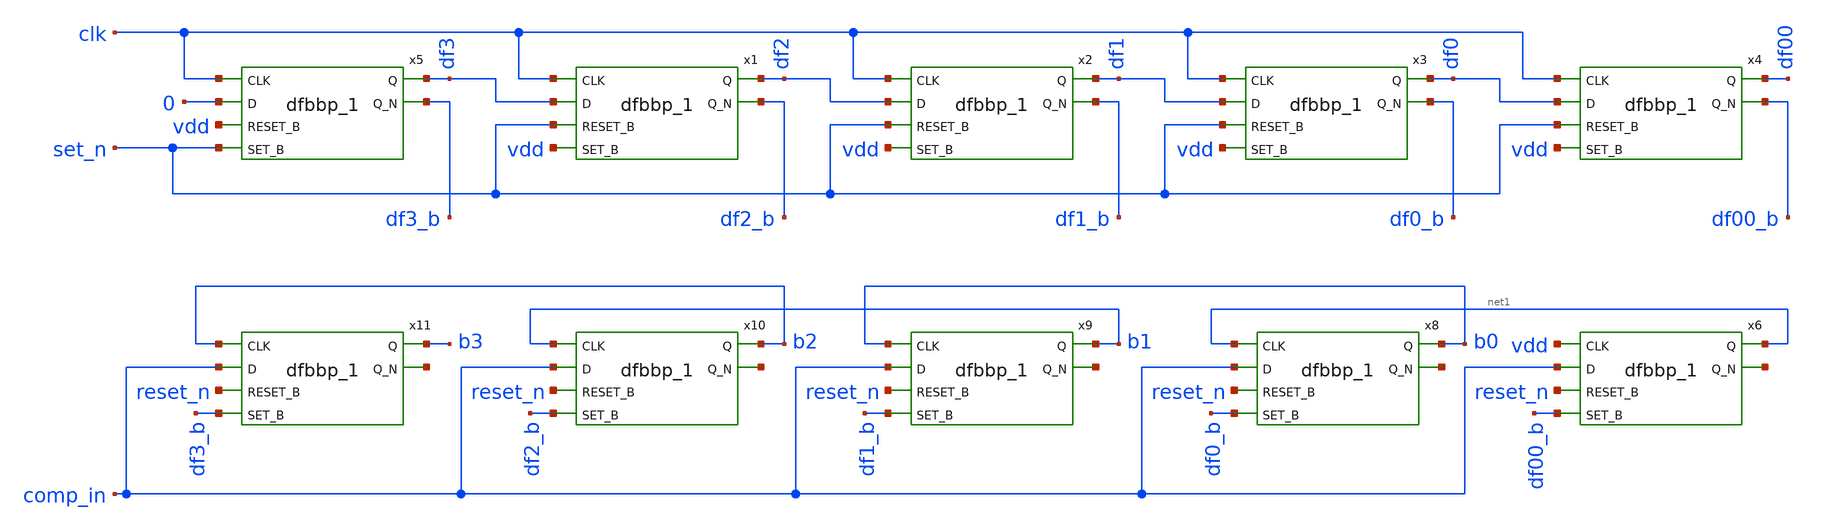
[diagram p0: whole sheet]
** sch_path: xschem/sar_logic/sarlogic_4bit.sch
**.subckt sarlogic_4bit
x5 clk 0 vdd set_n vss vss vcc vcc df3 df3_b sky130_fd_sc_hd__dfbbp_1
x1 clk df3 set_n vdd vss vss vcc vcc df2 df2_b sky130_fd_sc_hd__dfbbp_1
x2 clk df2 set_n vdd vss vss vcc vcc df1 df1_b sky130_fd_sc_hd__dfbbp_1
x3 clk df1 set_n vdd vss vss vcc vcc df0 df0_b sky130_fd_sc_hd__dfbbp_1
x4 clk df0 set_n vdd vss vss vcc vcc df00 df00_b sky130_fd_sc_hd__dfbbp_1
x6 vdd comp_in reset_n df00_b vss vss vcc vcc net1 net2 sky130_fd_sc_hd__dfbbp_1
x8 net1 comp_in reset_n df0_b vss vss vcc vcc b0 net3 sky130_fd_sc_hd__dfbbp_1
x9 b0 comp_in reset_n df1_b vss vss vcc vcc b1 net4 sky130_fd_sc_hd__dfbbp_1
x10 b1 comp_in reset_n df2_b vss vss vcc vcc b2 net5 sky130_fd_sc_hd__dfbbp_1
x11 b2 comp_in reset_n df3_b vss vss vcc vcc b3 net6 sky130_fd_sc_hd__dfbbp_1
**.ends
.end
